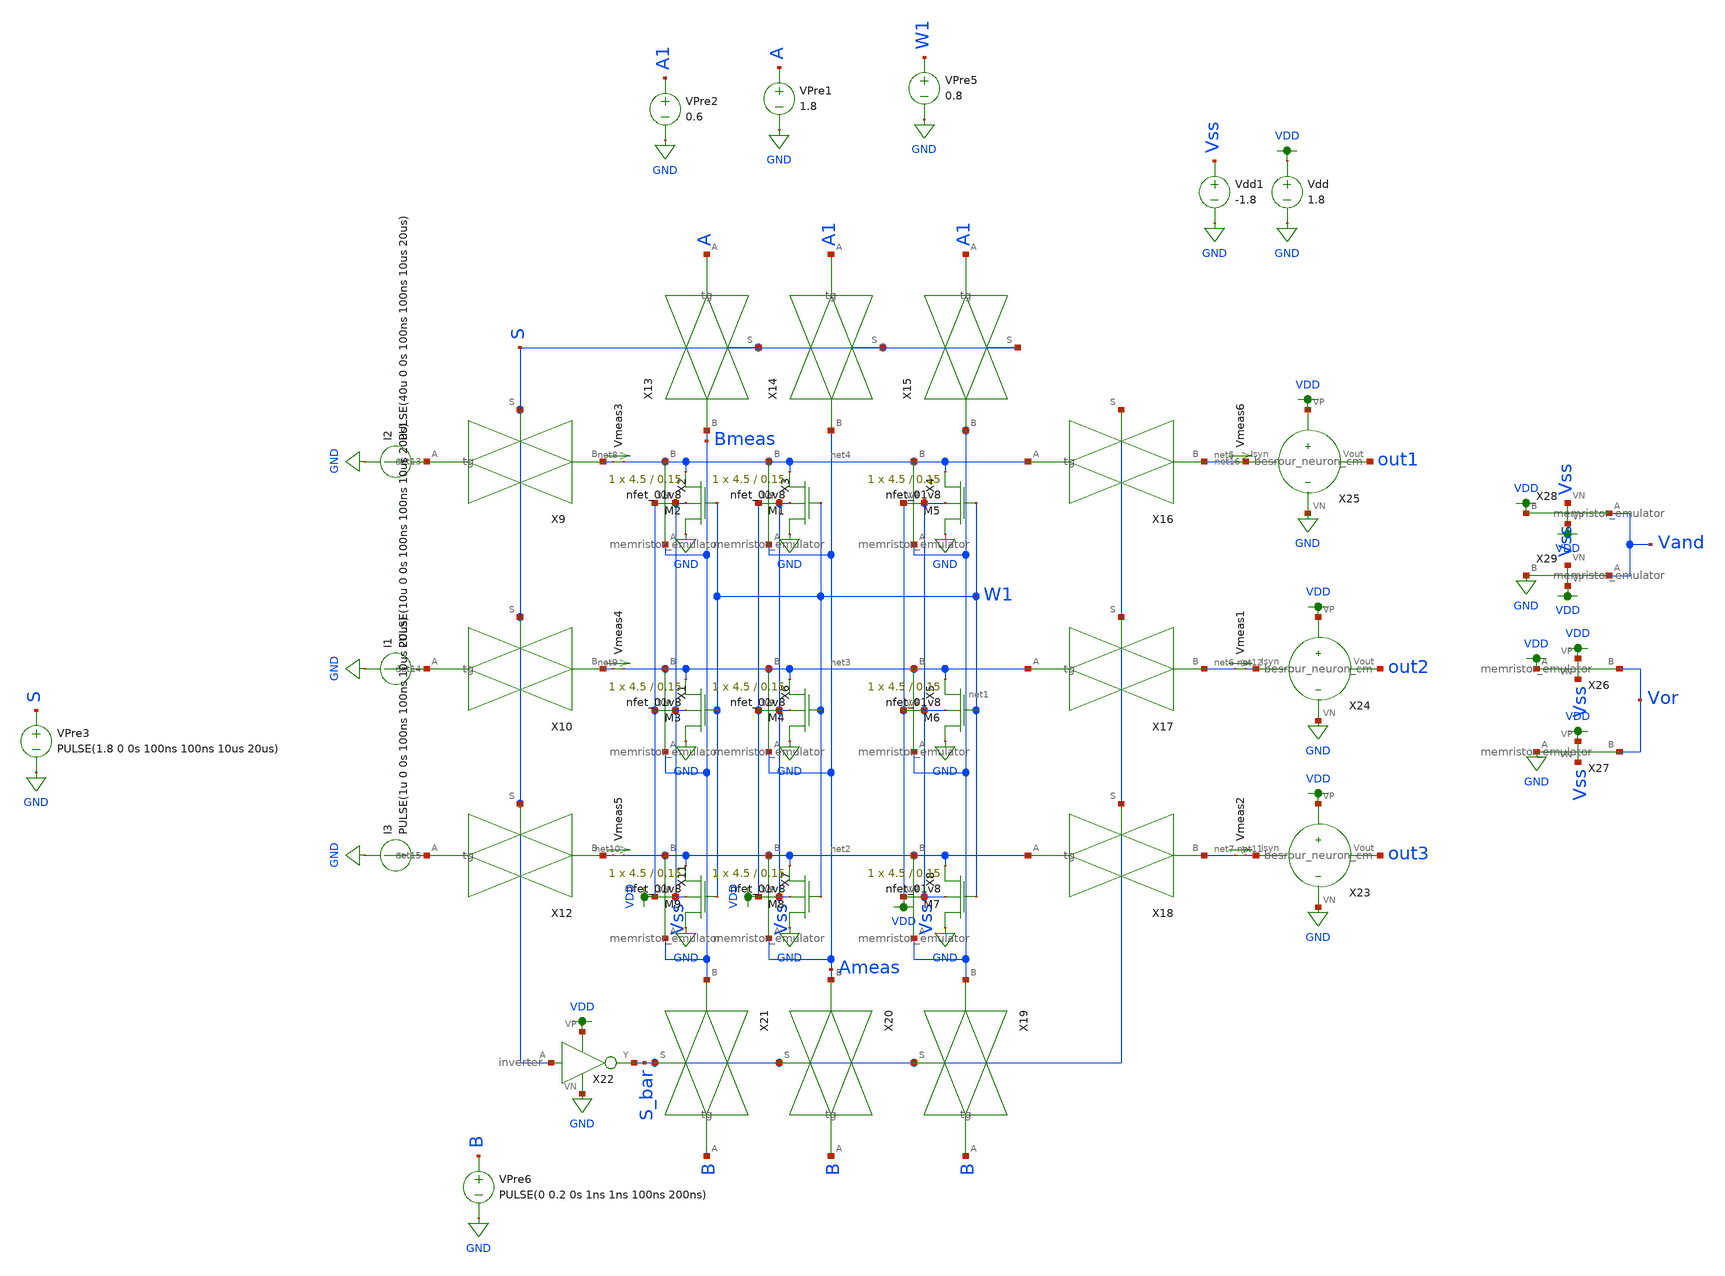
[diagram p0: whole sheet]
** sch_path: schematic/crossbar.sch
**.subckt crossbar
Vdd VDD GND 1.8
Vdd1 Vss GND -1.8
X11 VDD Vss net2 Bmeas memristor_emulator
X1 VDD Vss net3 Bmeas memristor_emulator
X2 VDD Vss net4 Bmeas memristor_emulator
X3 VDD Vss net4 Ameas memristor_emulator
X4 VDD Vss net4 net1 memristor_emulator
X5 VDD Vss net3 net1 memristor_emulator
X6 VDD Vss net3 Ameas memristor_emulator
X7 VDD Vss net2 Ameas memristor_emulator
X8 VDD Vss net2 net1 memristor_emulator
X9 S net13 net8 tg
X10 S net14 net9 tg
X12 S net15 net10 tg
X13 S A Bmeas tg
X14 S A1 Ameas tg
X15 S A1 net1 tg
X16 S_bar net4 net5 tg
X17 S_bar net3 net6 tg
X18 S_bar net2 net7 tg
X19 S_bar B net1 tg
X20 S_bar B Ameas tg
X21 S_bar B Bmeas tg
X22 S GND VDD S_bar inverter
VPre1 A GND 1.8
I2 GND net13 PULSE(40u 0 0s 100ns 100ns 10us 20us)
I1 GND net14 PULSE(10u 0 0s 100ns 100ns 10us 20us)
I3 GND net15 PULSE(1u 0 0s 100ns 100ns 10us 20us)
Vmeas1 net6 net12 0
.save i(vmeas1)
Vmeas2 net7 net11 0
.save i(vmeas2)
VPre3 S GND PULSE(1.8 0 0s 100ns 100ns 10us 20us)
Vmeas3 net8 net4 0
.save i(vmeas3)
Vmeas4 net9 net3 0
.save i(vmeas4)
Vmeas5 net10 net2 0
.save i(vmeas5)
X23 net11 out3 VDD GND besrour_neuron_cm
X24 net12 out2 VDD GND besrour_neuron_cm
X25 net16 out1 VDD GND besrour_neuron_cm
Vmeas6 net5 net16 0
.save i(vmeas6)
XM5 GND W1 net4 Vss sky130_fd_pr__nfet_01v8 L=0.15 W=4.5 nf=1 ad='int((nf+1)/2) * W/nf * 0.29' as='int((nf+2)/2) * W/nf * 0.29'
+ pd='2*int((nf+1)/2) * (W/nf + 0.29)' ps='2*int((nf+2)/2) * (W/nf + 0.29)' nrd='0.29 / W' nrs='0.29 / W'
+ sa=0 sb=0 sd=0 mult=1 m=1
XM1 GND W1 net4 Vss sky130_fd_pr__nfet_01v8 L=0.15 W=4.5 nf=1 ad='int((nf+1)/2) * W/nf * 0.29' as='int((nf+2)/2) * W/nf * 0.29'
+ pd='2*int((nf+1)/2) * (W/nf + 0.29)' ps='2*int((nf+2)/2) * (W/nf + 0.29)' nrd='0.29 / W' nrs='0.29 / W'
+ sa=0 sb=0 sd=0 mult=1 m=1
XM2 GND W1 net4 Vss sky130_fd_pr__nfet_01v8 L=0.15 W=4.5 nf=1 ad='int((nf+1)/2) * W/nf * 0.29' as='int((nf+2)/2) * W/nf * 0.29'
+ pd='2*int((nf+1)/2) * (W/nf + 0.29)' ps='2*int((nf+2)/2) * (W/nf + 0.29)' nrd='0.29 / W' nrs='0.29 / W'
+ sa=0 sb=0 sd=0 mult=1 m=1
XM3 GND W1 net3 Vss sky130_fd_pr__nfet_01v8 L=0.15 W=4.5 nf=1 ad='int((nf+1)/2) * W/nf * 0.29' as='int((nf+2)/2) * W/nf * 0.29'
+ pd='2*int((nf+1)/2) * (W/nf + 0.29)' ps='2*int((nf+2)/2) * (W/nf + 0.29)' nrd='0.29 / W' nrs='0.29 / W'
+ sa=0 sb=0 sd=0 mult=1 m=1
XM4 GND W1 net3 Vss sky130_fd_pr__nfet_01v8 L=0.15 W=4.5 nf=1 ad='int((nf+1)/2) * W/nf * 0.29' as='int((nf+2)/2) * W/nf * 0.29'
+ pd='2*int((nf+1)/2) * (W/nf + 0.29)' ps='2*int((nf+2)/2) * (W/nf + 0.29)' nrd='0.29 / W' nrs='0.29 / W'
+ sa=0 sb=0 sd=0 mult=1 m=1
XM6 GND W1 net3 Vss sky130_fd_pr__nfet_01v8 L=0.15 W=4.5 nf=1 ad='int((nf+1)/2) * W/nf * 0.29' as='int((nf+2)/2) * W/nf * 0.29'
+ pd='2*int((nf+1)/2) * (W/nf + 0.29)' ps='2*int((nf+2)/2) * (W/nf + 0.29)' nrd='0.29 / W' nrs='0.29 / W'
+ sa=0 sb=0 sd=0 mult=1 m=1
XM7 GND W1 net2 Vss sky130_fd_pr__nfet_01v8 L=0.15 W=4.5 nf=1 ad='int((nf+1)/2) * W/nf * 0.29' as='int((nf+2)/2) * W/nf * 0.29'
+ pd='2*int((nf+1)/2) * (W/nf + 0.29)' ps='2*int((nf+2)/2) * (W/nf + 0.29)' nrd='0.29 / W' nrs='0.29 / W'
+ sa=0 sb=0 sd=0 mult=1 m=1
XM8 GND W1 net2 Vss sky130_fd_pr__nfet_01v8 L=0.15 W=4.5 nf=1 ad='int((nf+1)/2) * W/nf * 0.29' as='int((nf+2)/2) * W/nf * 0.29'
+ pd='2*int((nf+1)/2) * (W/nf + 0.29)' ps='2*int((nf+2)/2) * (W/nf + 0.29)' nrd='0.29 / W' nrs='0.29 / W'
+ sa=0 sb=0 sd=0 mult=1 m=1
XM9 GND W1 net2 Vss sky130_fd_pr__nfet_01v8 L=0.15 W=4.5 nf=1 ad='int((nf+1)/2) * W/nf * 0.29' as='int((nf+2)/2) * W/nf * 0.29'
+ pd='2*int((nf+1)/2) * (W/nf + 0.29)' ps='2*int((nf+2)/2) * (W/nf + 0.29)' nrd='0.29 / W' nrs='0.29 / W'
+ sa=0 sb=0 sd=0 mult=1 m=1
VPre5 W1 GND 0.8
VPre6 B GND PULSE(0 0.2 0s 1ns 1ns 100ns 200ns)
VPre2 A1 GND 0.6
X26 VDD Vss Vor VDD memristor_emulator
X27 VDD Vss Vor GND memristor_emulator
X28 VDD Vss VDD Vand memristor_emulator
X29 VDD Vss GND Vand memristor_emulator
**** begin user architecture code

.option wnflag=1
.param MC_SWITCH=0.0
.lib ~/skywater/skywater-pdk/libraries/sky130_fd_pr_ngspice/latest/models/sky130.lib.spice tt


.param W=1
.param L=0.15
.tran 1n 50u
.save all

**** end user architecture code
**.ends

* expanding   symbol:  /home/madvlsi/neuromorphic_computing_final/schematic/memristor_emulator.sym #
*+ of pins=4
** sym_path: schematic/memristor_emulator.sym
** sch_path: schematic/memristor_emulator.sch
.subckt memristor_emulator VP VN B A
*.ipin A
*.iopin VN
*.iopin VP
*.opin B
XM1 B in_cap A B sky130_fd_pr__pfet_01v8 L=0.3 W=12 nf=1 ad='int((nf+1)/2) * W/nf * 0.29' as='int((nf+2)/2) * W/nf * 0.29'
+ pd='2*int((nf+1)/2) * (W/nf + 0.29)' ps='2*int((nf+2)/2) * (W/nf + 0.29)' nrd='0.29 / W' nrs='0.29 / W'
+ sa=0 sb=0 sd=0 mult=1 m=1
XM2 VP A in_cap VP sky130_fd_pr__pfet_01v8 L=2 W=3 nf=1 ad='int((nf+1)/2) * W/nf * 0.29' as='int((nf+2)/2) * W/nf * 0.29'
+ pd='2*int((nf+1)/2) * (W/nf + 0.29)' ps='2*int((nf+2)/2) * (W/nf + 0.29)' nrd='0.29 / W' nrs='0.29 / W'
+ sa=0 sb=0 sd=0 mult=1 m=1
XM3 VN in_cap VN VN sky130_fd_pr__nfet_01v8 L=20 W=20 nf=1 ad='int((nf+1)/2) * W/nf * 0.29' as='int((nf+2)/2) * W/nf * 0.29'
+ pd='2*int((nf+1)/2) * (W/nf + 0.29)' ps='2*int((nf+2)/2) * (W/nf + 0.29)' nrd='0.29 / W' nrs='0.29 / W'
+ sa=0 sb=0 sd=0 mult=1 m=1
XM4 VN B in_cap VN sky130_fd_pr__nfet_01v8 L=3 W=2 nf=1 ad='int((nf+1)/2) * W/nf * 0.29' as='int((nf+2)/2) * W/nf * 0.29'
+ pd='2*int((nf+1)/2) * (W/nf + 0.29)' ps='2*int((nf+2)/2) * (W/nf + 0.29)' nrd='0.29 / W' nrs='0.29 / W'
+ sa=0 sb=0 sd=0 mult=1 m=1
.ends


* expanding   symbol:  /home/madvlsi/neuromorphic_computing_final/schematic/tg.sym # of pins=3
** sym_path: schematic/tg.sym
** sch_path: schematic/tg.sch
.subckt tg S A B
*.ipin S
*.iopin B
*.iopin A
X1 S GND VDD net1 inverter
XM1 B net1 A VDD sky130_fd_pr__pfet_01v8 L=0.3 W=6 nf=1 ad='int((nf+1)/2) * W/nf * 0.29' as='int((nf+2)/2) * W/nf * 0.29'
+ pd='2*int((nf+1)/2) * (W/nf + 0.29)' ps='2*int((nf+2)/2) * (W/nf + 0.29)' nrd='0.29 / W' nrs='0.29 / W'
+ sa=0 sb=0 sd=0 mult=1 m=1
XM2 B S A GND sky130_fd_pr__nfet_01v8 L=0.3 W=6 nf=1 ad='int((nf+1)/2) * W/nf * 0.29' as='int((nf+2)/2) * W/nf * 0.29'
+ pd='2*int((nf+1)/2) * (W/nf + 0.29)' ps='2*int((nf+2)/2) * (W/nf + 0.29)' nrd='0.29 / W' nrs='0.29 / W'
+ sa=0 sb=0 sd=0 mult=1 m=1
.ends


* expanding   symbol:  /home/madvlsi/neuromorphic_computing_final/schematic/inverter.sym # of pins=4
** sym_path: schematic/inverter.sym
** sch_path: schematic/inverter.sch
.subckt inverter A VN VP Y
*.ipin A
*.iopin VP
*.iopin VN
*.opin Y
XM1 Y A VN VN sky130_fd_pr__nfet_01v8 L=0.15 W=1 nf=1 ad='int((nf+1)/2) * W/nf * 0.29' as='int((nf+2)/2) * W/nf * 0.29'
+ pd='2*int((nf+1)/2) * (W/nf + 0.29)' ps='2*int((nf+2)/2) * (W/nf + 0.29)' nrd='0.29 / W' nrs='0.29 / W'
+ sa=0 sb=0 sd=0 mult=1 m=1
XM2 Y A VP VP sky130_fd_pr__pfet_01v8 L=0.15 W=1 nf=1 ad='int((nf+1)/2) * W/nf * 0.29' as='int((nf+2)/2) * W/nf * 0.29'
+ pd='2*int((nf+1)/2) * (W/nf + 0.29)' ps='2*int((nf+2)/2) * (W/nf + 0.29)' nrd='0.29 / W' nrs='0.29 / W'
+ sa=0 sb=0 sd=0 mult=1 m=1
.ends


* expanding   symbol:  /home/madvlsi/neuromorphic_computing_final/schematic/besrour_neuron_cm.sym #
*+ of pins=4
** sym_path: schematic/besrour_neuron_cm.sym
** sch_path: schematic/besrour_neuron_cm.sch
.subckt besrour_neuron_cm Isyn Vout VP VN
*.iopin VP
*.iopin VN
*.iopin Isyn
*.opin Vout
XM2 VMEMINT net1 VP VDD sky130_fd_pr__pfet_01v8 L={L} W={W} nf=1 ad='int((nf+1)/2) * W/nf * 0.29' as='int((nf+2)/2) * W/nf * 0.29'
+ pd='2*int((nf+1)/2) * (W/nf + 0.29)' ps='2*int((nf+2)/2) * (W/nf + 0.29)' nrd='0.29 / W' nrs='0.29 / W'
+ sa=0 sb=0 sd=0 mult=1 m=1
XM3 VP net3 VMEMINT VDD sky130_fd_pr__pfet_01v8 L={L} W={W} nf=1 ad='int((nf+1)/2) * W/nf * 0.29' as='int((nf+2)/2) * W/nf * 0.29'
+ pd='2*int((nf+1)/2) * (W/nf + 0.29)' ps='2*int((nf+2)/2) * (W/nf + 0.29)' nrd='0.29 / W' nrs='0.29 / W'
+ sa=0 sb=0 sd=0 mult=1 m=1
XM4 net3 VMEMINT VP VDD sky130_fd_pr__pfet_01v8 L={L} W={W} nf=1 ad='int((nf+1)/2) * W/nf * 0.29' as='int((nf+2)/2) * W/nf * 0.29'
+ pd='2*int((nf+1)/2) * (W/nf + 0.29)' ps='2*int((nf+2)/2) * (W/nf + 0.29)' nrd='0.29 / W' nrs='0.29 / W'
+ sa=0 sb=0 sd=0 mult=1 m=1
XM5 net2 net3 VP VDD sky130_fd_pr__pfet_01v8 L={L} W={W} nf=1 ad='int((nf+1)/2) * W/nf * 0.29' as='int((nf+2)/2) * W/nf * 0.29'
+ pd='2*int((nf+1)/2) * (W/nf + 0.29)' ps='2*int((nf+2)/2) * (W/nf + 0.29)' nrd='0.29 / W' nrs='0.29 / W'
+ sa=0 sb=0 sd=0 mult=1 m=1
XM6 net3 VMEMINT VN GND sky130_fd_pr__nfet_01v8 L={L} W={W} nf=1 ad='int((nf+1)/2) * W/nf * 0.29' as='int((nf+2)/2) * W/nf * 0.29'
+ pd='2*int((nf+1)/2) * (W/nf + 0.29)' ps='2*int((nf+2)/2) * (W/nf + 0.29)' nrd='0.29 / W' nrs='0.29 / W'
+ sa=0 sb=0 sd=0 mult=1 m=1
XM8 net2 net3 VN GND sky130_fd_pr__nfet_01v8 L={L} W={W} nf=1 ad='int((nf+1)/2) * W/nf * 0.29' as='int((nf+2)/2) * W/nf * 0.29'
+ pd='2*int((nf+1)/2) * (W/nf + 0.29)' ps='2*int((nf+2)/2) * (W/nf + 0.29)' nrd='0.29 / W' nrs='0.29 / W'
+ sa=0 sb=0 sd=0 mult=1 m=1
C1 VMEMINT VN 340f m=1
C2 net2 VN 340f m=1
XM9 net4 net2 VP VDD sky130_fd_pr__pfet_01v8 L={L} W={W} nf=1 ad='int((nf+1)/2) * W/nf * 0.29' as='int((nf+2)/2) * W/nf * 0.29'
+ pd='2*int((nf+1)/2) * (W/nf + 0.29)' ps='2*int((nf+2)/2) * (W/nf + 0.29)' nrd='0.29 / W' nrs='0.29 / W'
+ sa=0 sb=0 sd=0 mult=1 m=1
XM10 net4 net2 VN GND sky130_fd_pr__nfet_01v8 L={L} W={W} nf=1 ad='int((nf+1)/2) * W/nf * 0.29' as='int((nf+2)/2) * W/nf * 0.29'
+ pd='2*int((nf+1)/2) * (W/nf + 0.29)' ps='2*int((nf+2)/2) * (W/nf + 0.29)' nrd='0.29 / W' nrs='0.29 / W'
+ sa=0 sb=0 sd=0 mult=1 m=1
XM11 Vout net4 VP VDD sky130_fd_pr__pfet_01v8 L={L} W={W} nf=1 ad='int((nf+1)/2) * W/nf * 0.29' as='int((nf+2)/2) * W/nf * 0.29'
+ pd='2*int((nf+1)/2) * (W/nf + 0.29)' ps='2*int((nf+2)/2) * (W/nf + 0.29)' nrd='0.29 / W' nrs='0.29 / W'
+ sa=0 sb=0 sd=0 mult=1 m=1
XM12 Vout net4 VN GND sky130_fd_pr__nfet_01v8 L={L} W={W} nf=1 ad='int((nf+1)/2) * W/nf * 0.29' as='int((nf+2)/2) * W/nf * 0.29'
+ pd='2*int((nf+1)/2) * (W/nf + 0.29)' ps='2*int((nf+2)/2) * (W/nf + 0.29)' nrd='0.29 / W' nrs='0.29 / W'
+ sa=0 sb=0 sd=0 mult=1 m=1
XM13 net1 Isyn VN GND sky130_fd_pr__nfet_01v8 L={L} W={W} nf=1 ad='int((nf+1)/2) * W/nf * 0.29' as='int((nf+2)/2) * W/nf * 0.29'
+ pd='2*int((nf+1)/2) * (W/nf + 0.29)' ps='2*int((nf+2)/2) * (W/nf + 0.29)' nrd='0.29 / W' nrs='0.29 / W'
+ sa=0 sb=0 sd=0 mult=1 m=1
XM14 VN Isyn Isyn GND sky130_fd_pr__nfet_01v8 L={L} W={W} nf=1 ad='int((nf+1)/2) * W/nf * 0.29' as='int((nf+2)/2) * W/nf * 0.29'
+ pd='2*int((nf+1)/2) * (W/nf + 0.29)' ps='2*int((nf+2)/2) * (W/nf + 0.29)' nrd='0.29 / W' nrs='0.29 / W'
+ sa=0 sb=0 sd=0 mult=1 m=1
XM1 VP net1 net1 VDD sky130_fd_pr__pfet_01v8 L={L} W={W} nf=1 ad='int((nf+1)/2) * W/nf * 0.29' as='int((nf+2)/2) * W/nf * 0.29'
+ pd='2*int((nf+1)/2) * (W/nf + 0.29)' ps='2*int((nf+2)/2) * (W/nf + 0.29)' nrd='0.29 / W' nrs='0.29 / W'
+ sa=0 sb=0 sd=0 mult=1 m=1
XM7 VN net2 VMEMINT GND sky130_fd_pr__nfet_01v8 L={L} W={W} nf=1 ad='int((nf+1)/2) * W/nf * 0.29' as='int((nf+2)/2) * W/nf * 0.29'
+ pd='2*int((nf+1)/2) * (W/nf + 0.29)' ps='2*int((nf+2)/2) * (W/nf + 0.29)' nrd='0.29 / W' nrs='0.29 / W'
+ sa=0 sb=0 sd=0 mult=1 m=1
.ends

.GLOBAL VDD
.GLOBAL GND
.end
